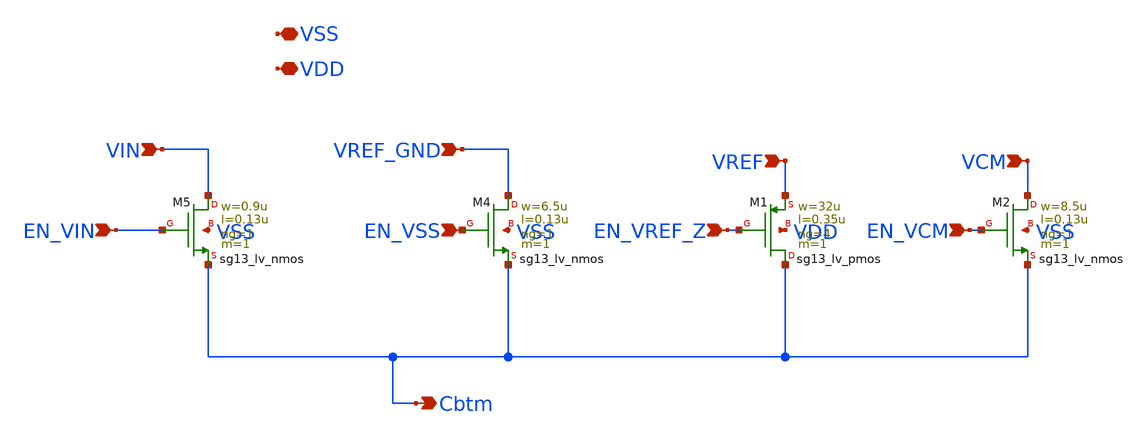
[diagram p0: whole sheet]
** sch_path: schematic/individual_switches/switch_C8.sch
**.subckt switch_C8 VIN EN_VIN VREF_GND EN_VSS Cbtm VSS VREF EN_VREF_Z EN_VCM VCM VDD
*.ipin VIN
*.ipin EN_VIN
*.ipin VREF_GND
*.ipin EN_VSS
*.opin Cbtm
*.iopin VSS
*.ipin VREF
*.ipin EN_VREF_Z
*.ipin EN_VCM
*.ipin VCM
*.iopin VDD
XM5 VIN EN_VIN Cbtm VSS sg13_lv_nmos w=0.9u l=0.13u ng=1 m=1 mm_ok=1
XM4 VREF_GND EN_VSS Cbtm VSS sg13_lv_nmos w=6.5u l=0.13u ng=1 m=1 mm_ok=1
XM1 Cbtm EN_VREF_Z VREF VDD sg13_lv_pmos w=32u l=0.35u ng=4 m=1 mm_ok=1
XM2 VCM EN_VCM Cbtm VSS sg13_lv_nmos w=8.5u l=0.13u ng=1 m=1 mm_ok=1
**.ends
.end
